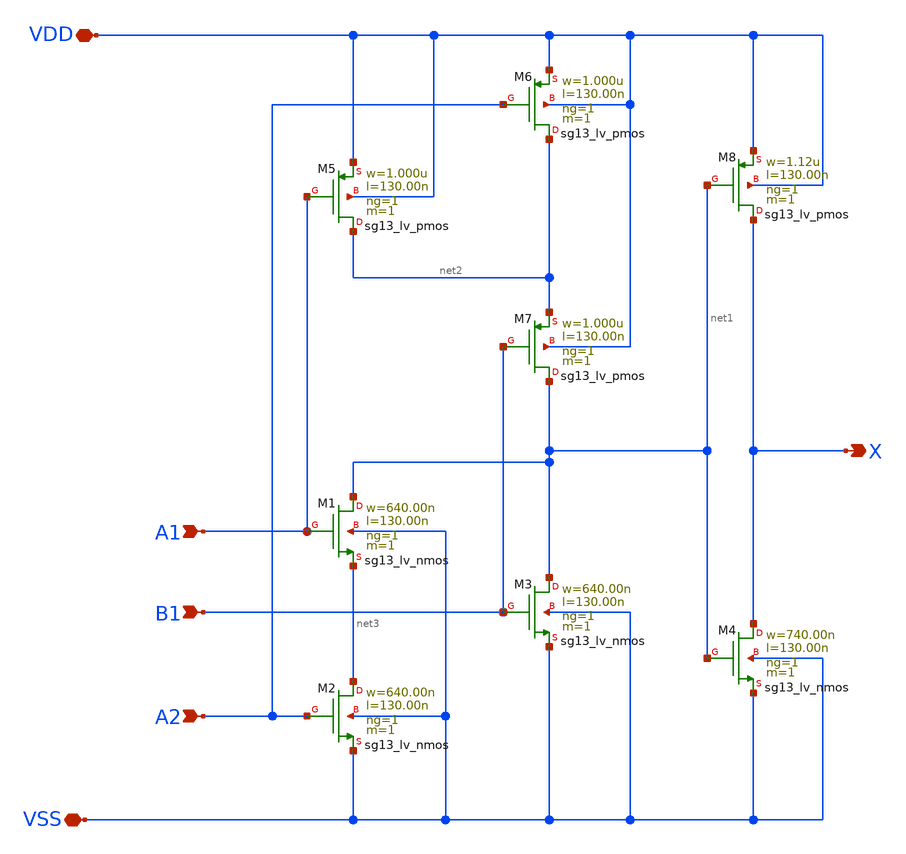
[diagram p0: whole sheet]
** sch_path: ihp-sg13g2/libs.tech/xschem/sg13g2_stdcells/sg13g2_a21o_1.sch
**.subckt sg13g2_a21o_1 X A1 A2 B1 VDD VSS
*.opin X
*.ipin A1
*.ipin A2
*.ipin B1
*.iopin VDD
*.iopin VSS
XM1 net1 A1 net3 VSS sg13_lv_nmos w=640.00n l=130.00n ng=1 m=1 mm_ok=1
XM2 net3 A2 VSS VSS sg13_lv_nmos w=640.00n l=130.00n ng=1 m=1 mm_ok=1
XM3 net1 B1 VSS VSS sg13_lv_nmos w=640.00n l=130.00n ng=1 m=1 mm_ok=1
XM4 X net1 VSS VSS sg13_lv_nmos w=740.00n l=130.00n ng=1 m=1 mm_ok=1
XM5 net2 A1 VDD VDD sg13_lv_pmos w=1.000u l=130.00n ng=1 m=1 mm_ok=1
XM6 net2 A2 VDD VDD sg13_lv_pmos w=1.000u l=130.00n ng=1 m=1 mm_ok=1
XM7 net1 B1 net2 VDD sg13_lv_pmos w=1.000u l=130.00n ng=1 m=1 mm_ok=1
XM8 X net1 VDD VDD sg13_lv_pmos w=1.12u l=130.00n ng=1 m=1 mm_ok=1
**.ends
.end
